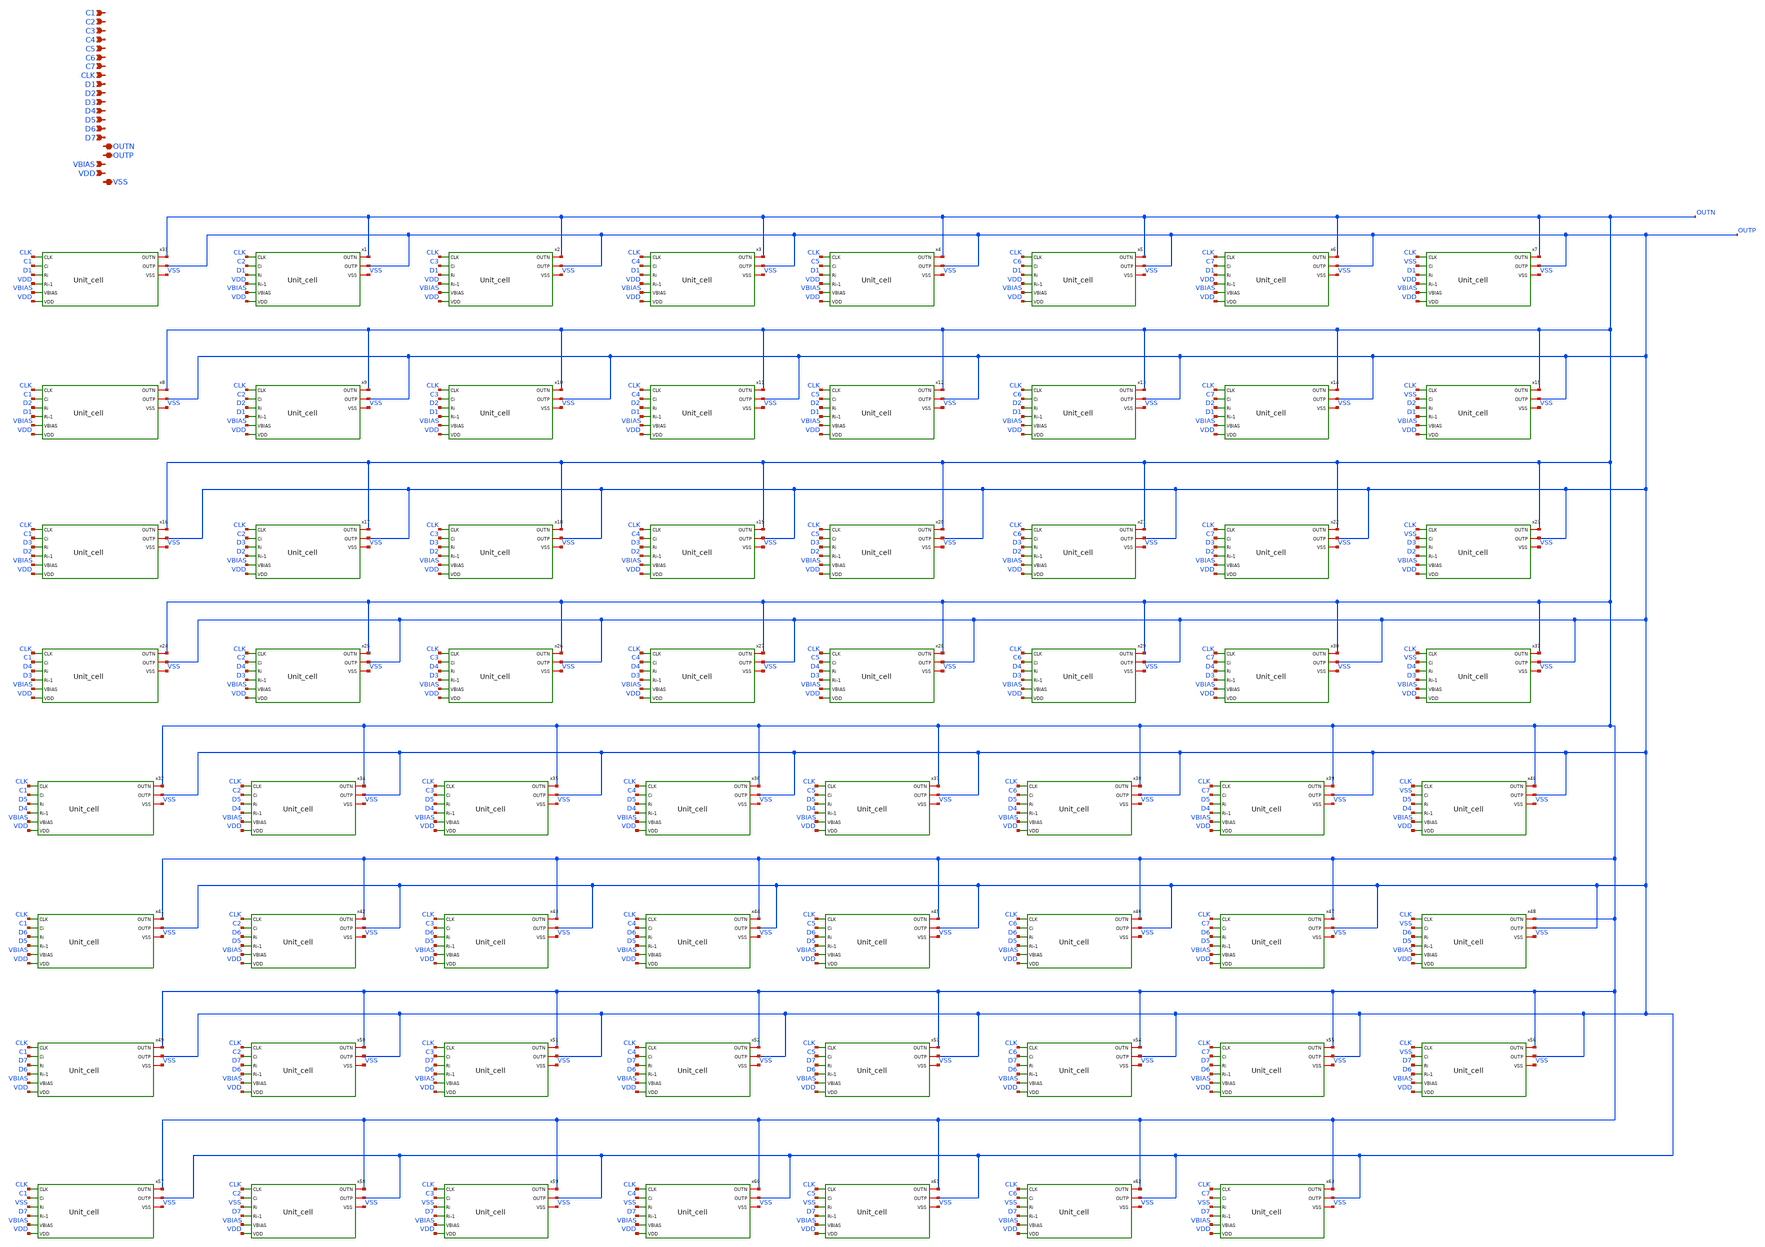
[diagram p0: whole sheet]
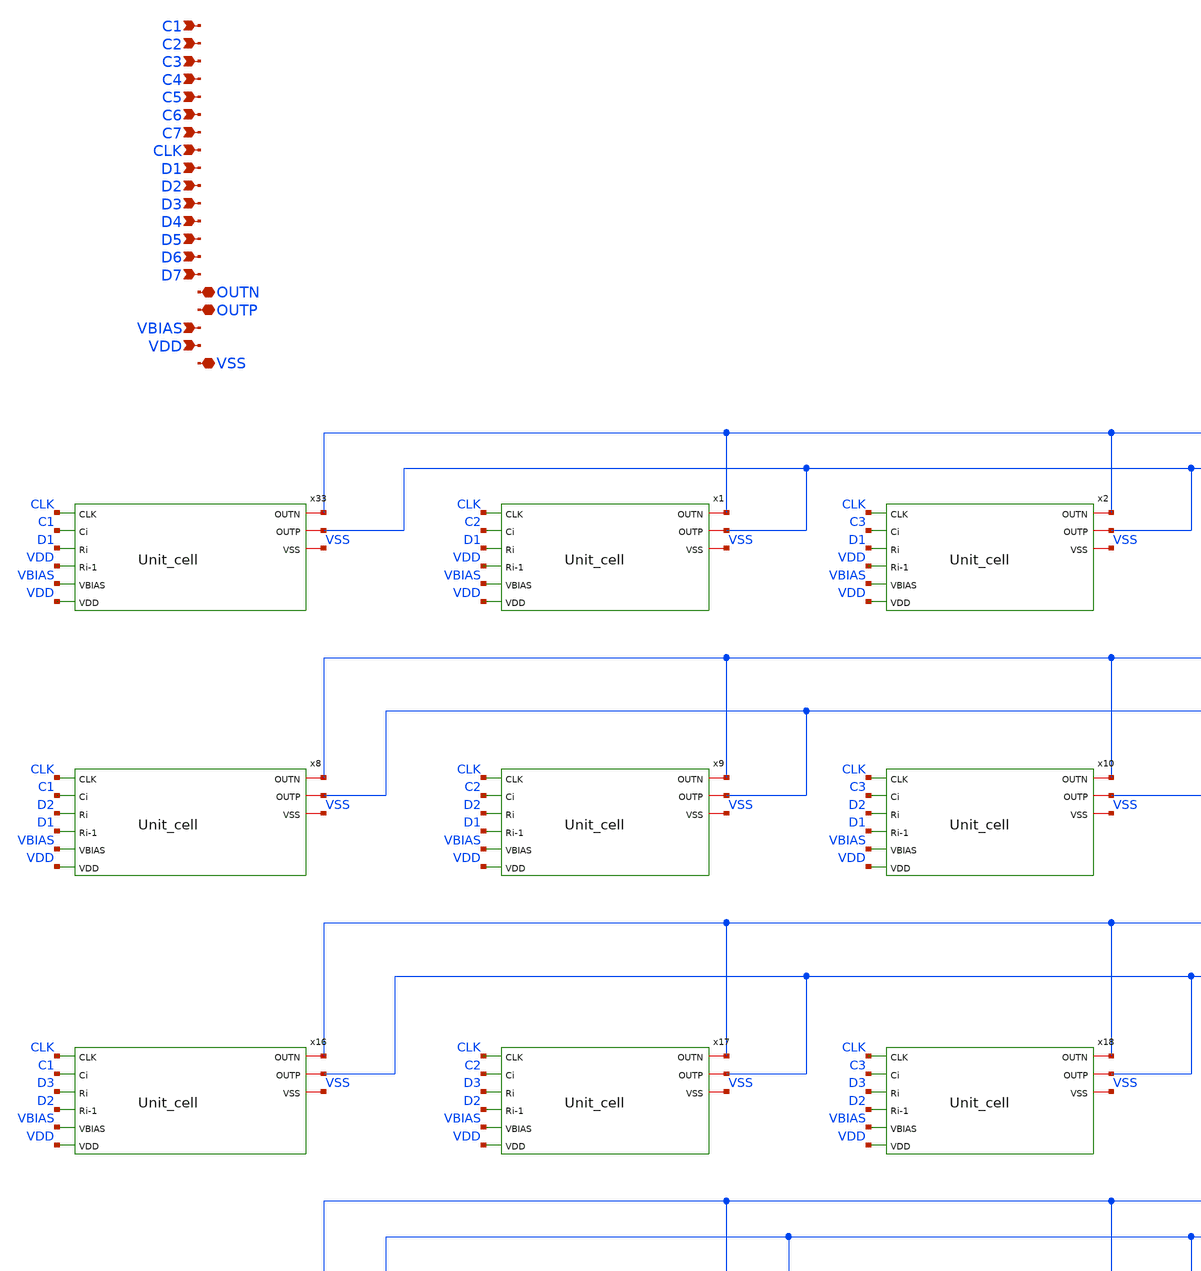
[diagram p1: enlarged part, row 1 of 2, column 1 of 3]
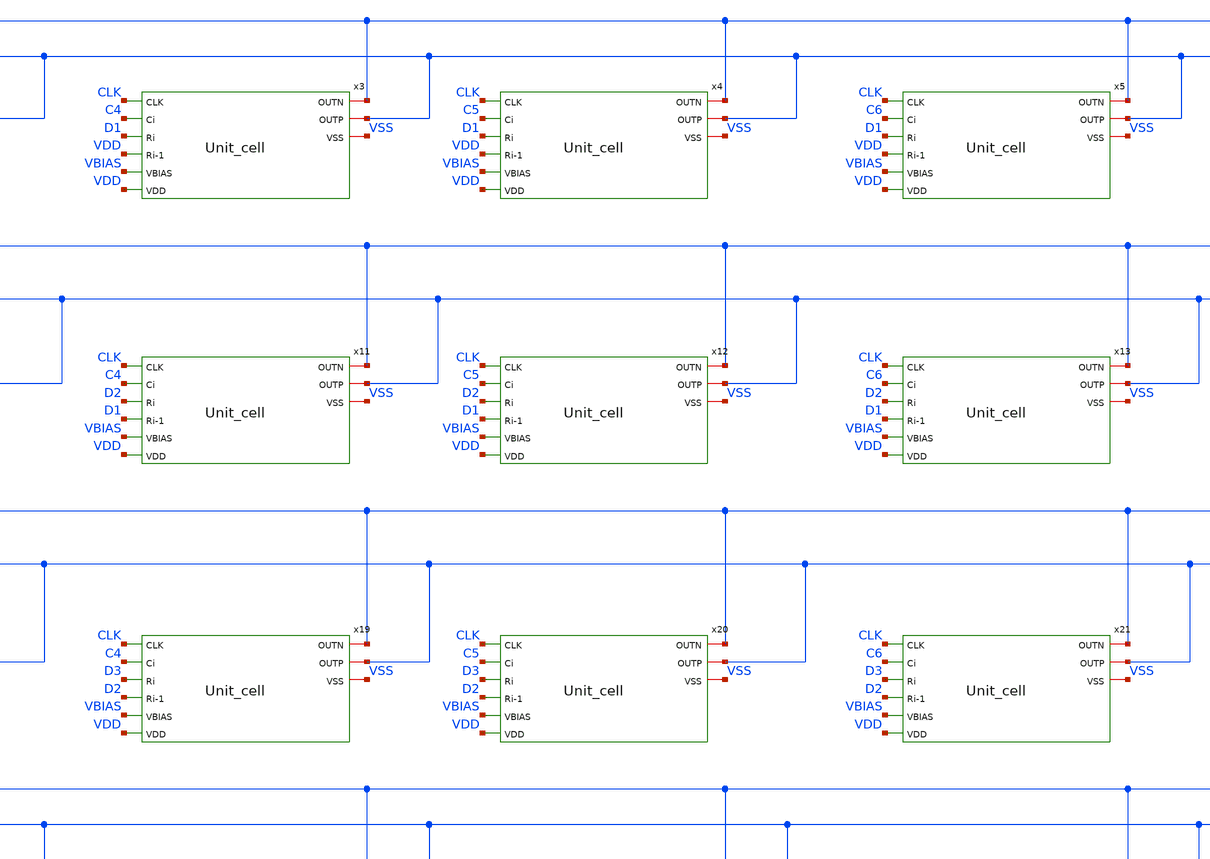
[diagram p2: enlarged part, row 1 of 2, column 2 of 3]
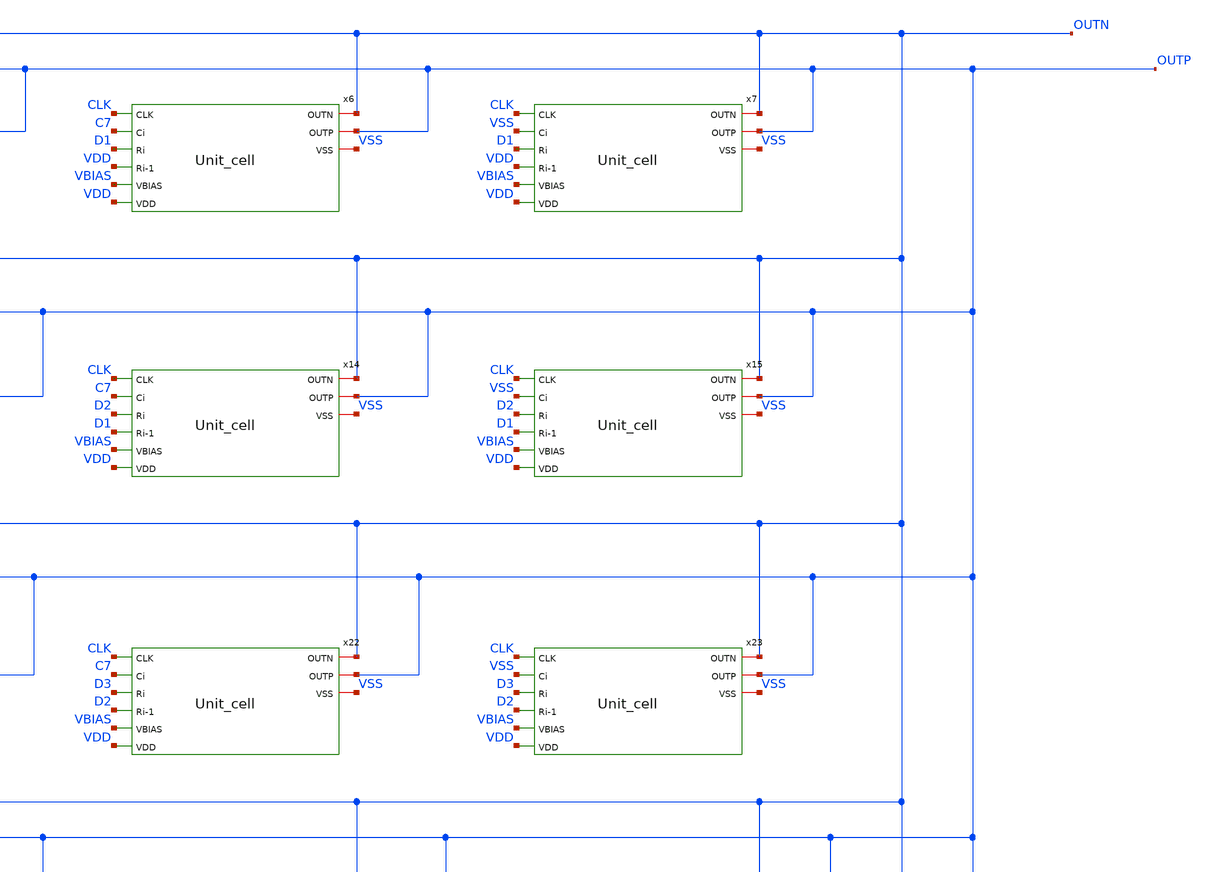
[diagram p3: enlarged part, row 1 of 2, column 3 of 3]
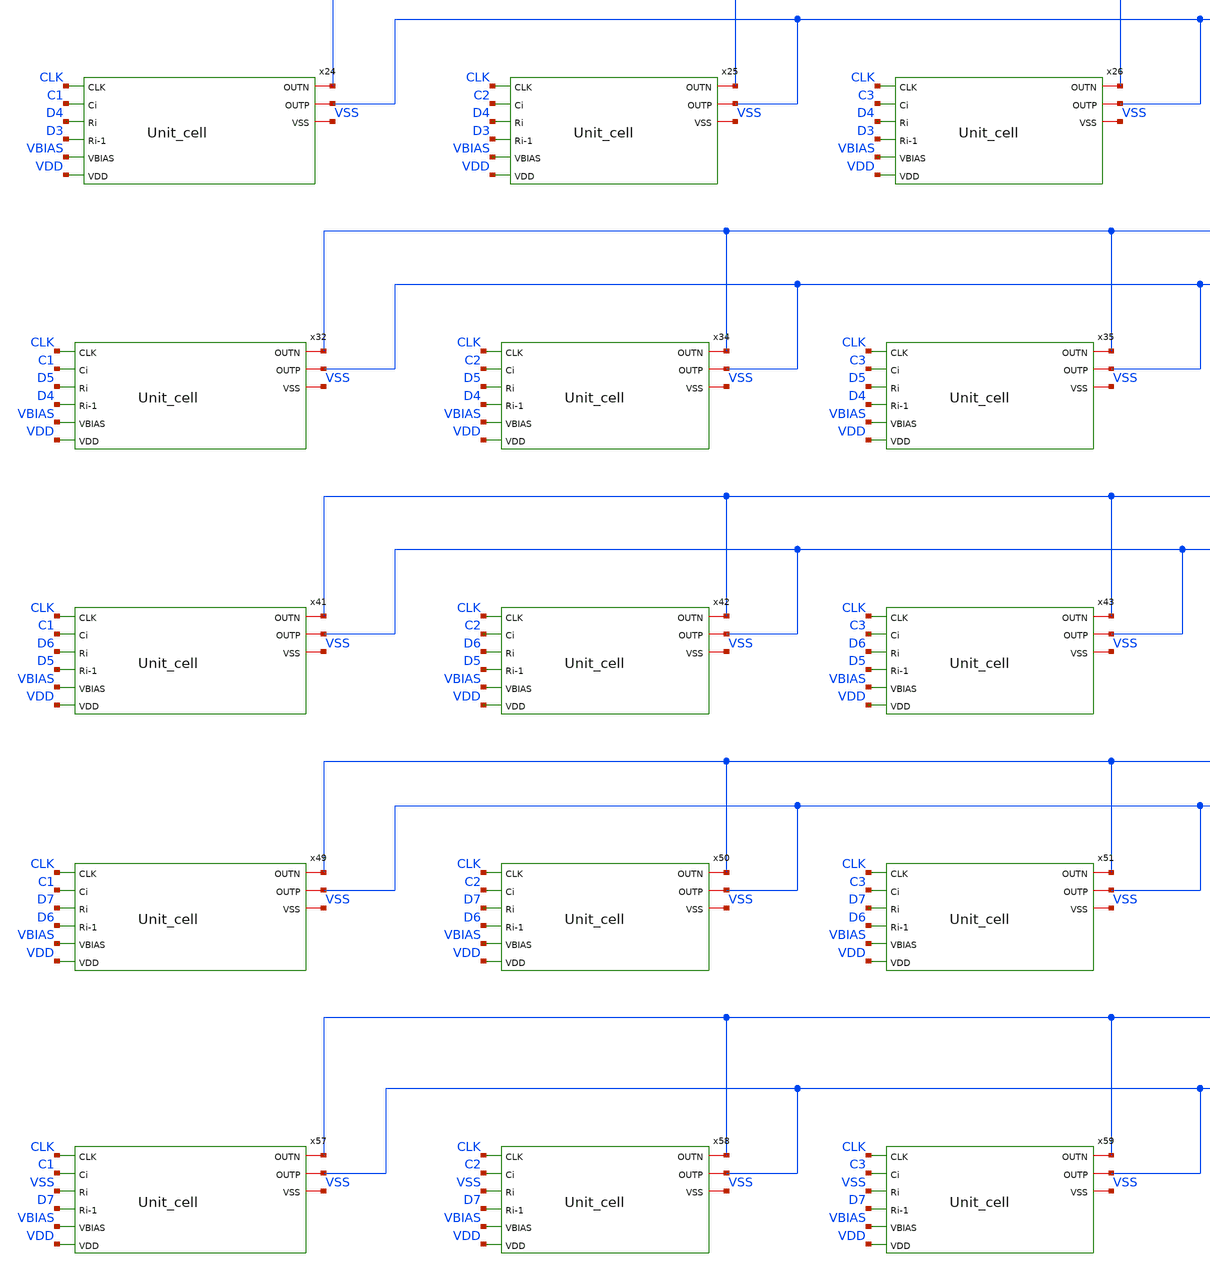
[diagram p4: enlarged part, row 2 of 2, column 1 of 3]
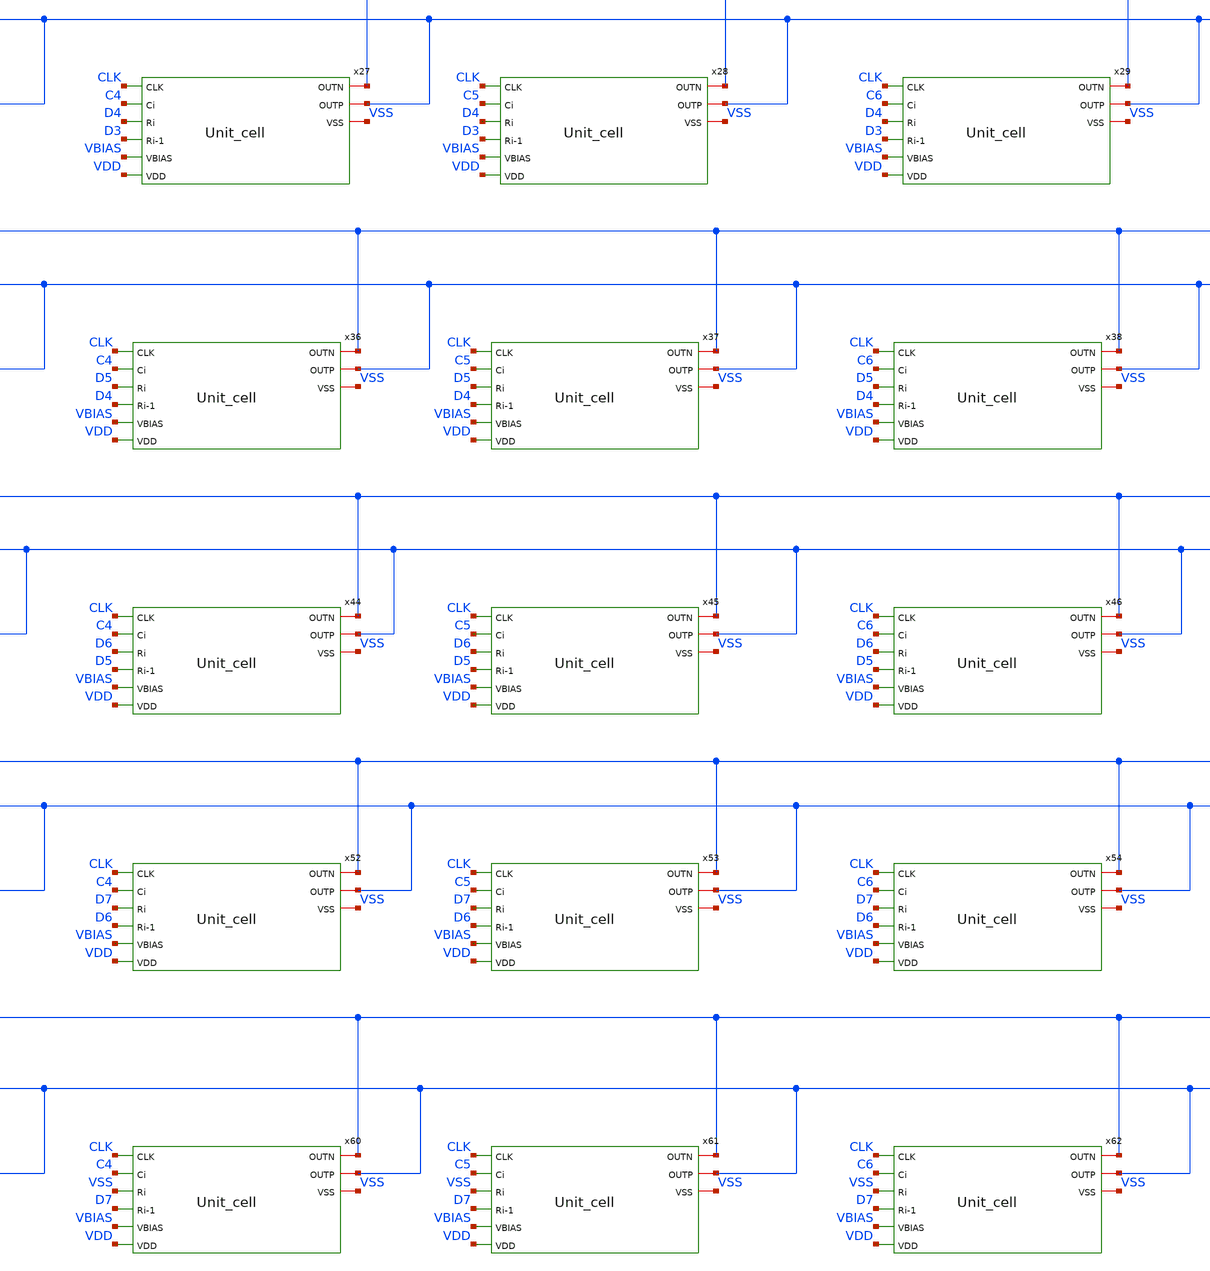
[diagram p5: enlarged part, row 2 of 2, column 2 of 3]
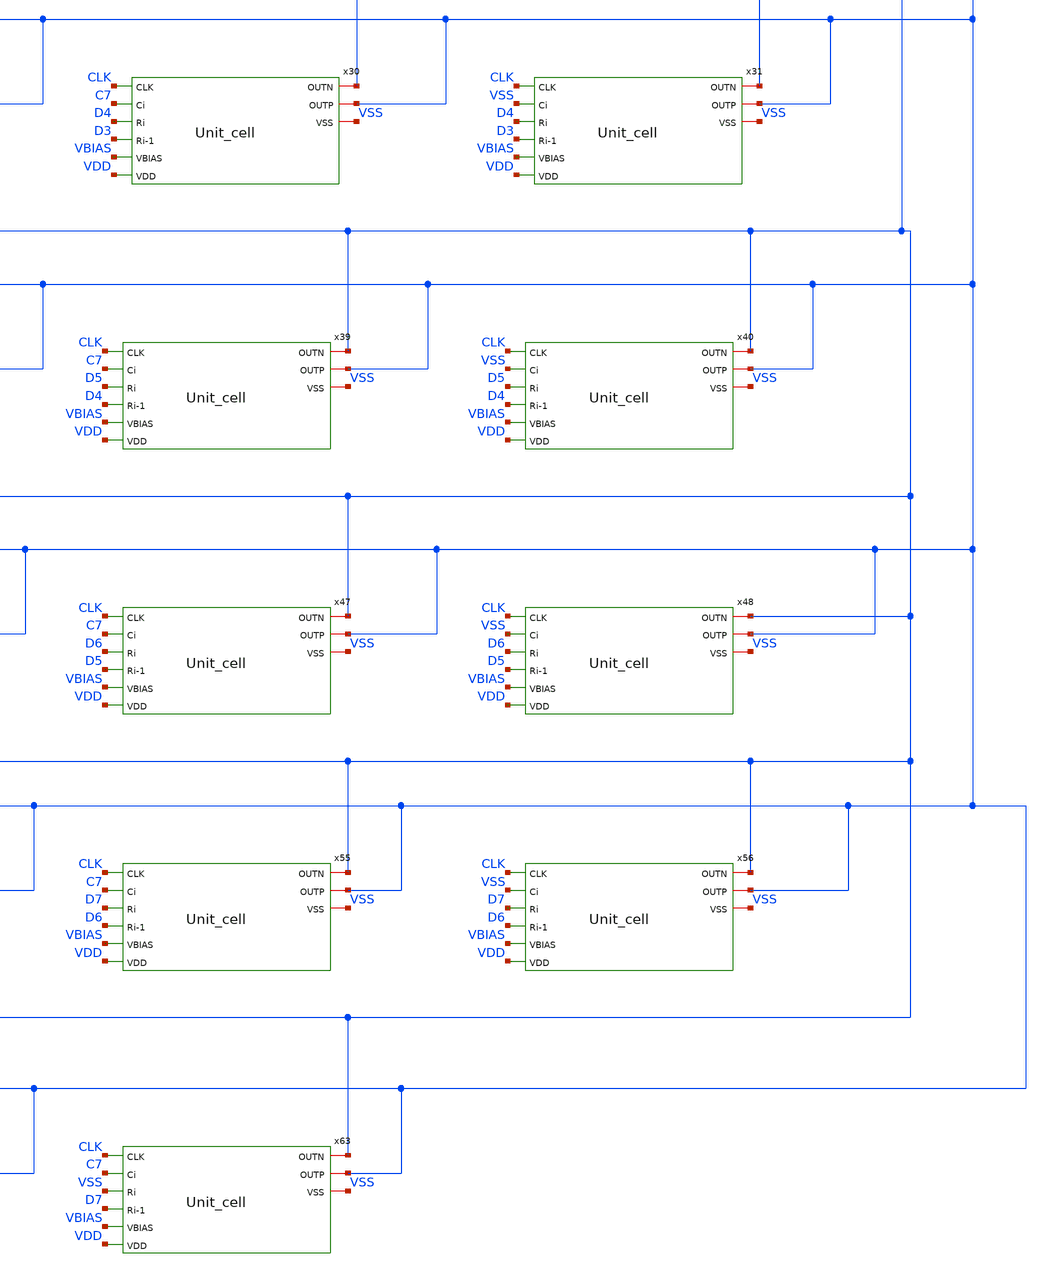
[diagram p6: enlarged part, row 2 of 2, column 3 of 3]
** sch_path: klayout/xschem/6MSB.sch
* IHP-GmbH/IHP-Open-PDK/ihp-sg13g2/libs.tech/xschem/sg13g2_stdcells/sg13g2_or2_2.sch:
* Copyright 2023 IHP PDK Authors
* Licensed under the Apache License, Version 2.0 (the "License");
**.subckt 6MSB VSS VDD VBIAS OUTP OUTN D7 D6 D5 D4 D3 D2 D1 CLK C7 C6 C5 C4 C3 C2 C1
*.iopin VSS
*.ipin VDD
*.ipin VBIAS
*.iopin OUTP
*.iopin OUTN
*.ipin D7
*.ipin D6
*.ipin D5
*.ipin D4
*.ipin D3
*.ipin D2
*.ipin D1
*.ipin CLK
*.ipin C7
*.ipin C6
*.ipin C5
*.ipin C4
*.ipin C3
*.ipin C2
*.ipin C1
x33 CLK C1 OUTN OUTP D1 VDD VBIAS VDD VSS Unit_cell
x1 CLK C2 OUTN OUTP D1 VDD VBIAS VDD VSS Unit_cell
x2 CLK C3 OUTN OUTP D1 VDD VBIAS VDD VSS Unit_cell
x3 CLK C4 OUTN OUTP D1 VDD VBIAS VDD VSS Unit_cell
x4 CLK C5 OUTN OUTP D1 VDD VBIAS VDD VSS Unit_cell
x5 CLK C6 OUTN OUTP D1 VDD VBIAS VDD VSS Unit_cell
x6 CLK C7 OUTN OUTP D1 VDD VBIAS VDD VSS Unit_cell
x7 CLK VSS OUTN OUTP D1 VDD VBIAS VDD VSS Unit_cell
x8 CLK C1 OUTN OUTP D2 D1 VBIAS VDD VSS Unit_cell
x9 CLK C2 OUTN OUTP D2 D1 VBIAS VDD VSS Unit_cell
x10 CLK C3 OUTN OUTP D2 D1 VBIAS VDD VSS Unit_cell
x11 CLK C4 OUTN OUTP D2 D1 VBIAS VDD VSS Unit_cell
x12 CLK C5 OUTN OUTP D2 D1 VBIAS VDD VSS Unit_cell
x13 CLK C6 OUTN OUTP D2 D1 VBIAS VDD VSS Unit_cell
x14 CLK C7 OUTN OUTP D2 D1 VBIAS VDD VSS Unit_cell
x15 CLK VSS OUTN OUTP D2 D1 VBIAS VDD VSS Unit_cell
x16 CLK C1 OUTN OUTP D3 D2 VBIAS VDD VSS Unit_cell
x17 CLK C2 OUTN OUTP D3 D2 VBIAS VDD VSS Unit_cell
x18 CLK C3 OUTN OUTP D3 D2 VBIAS VDD VSS Unit_cell
x19 CLK C4 OUTN OUTP D3 D2 VBIAS VDD VSS Unit_cell
x20 CLK C5 OUTN OUTP D3 D2 VBIAS VDD VSS Unit_cell
x21 CLK C6 OUTN OUTP D3 D2 VBIAS VDD VSS Unit_cell
x22 CLK C7 OUTN OUTP D3 D2 VBIAS VDD VSS Unit_cell
x23 CLK VSS OUTN OUTP D3 D2 VBIAS VDD VSS Unit_cell
x24 CLK C1 OUTN OUTP D4 D3 VBIAS VDD VSS Unit_cell
x25 CLK C2 OUTN OUTP D4 D3 VBIAS VDD VSS Unit_cell
x26 CLK C3 OUTN OUTP D4 D3 VBIAS VDD VSS Unit_cell
x27 CLK C4 OUTN OUTP D4 D3 VBIAS VDD VSS Unit_cell
x28 CLK C5 OUTN OUTP D4 D3 VBIAS VDD VSS Unit_cell
x29 CLK C6 OUTN OUTP D4 D3 VBIAS VDD VSS Unit_cell
x30 CLK C7 OUTN OUTP D4 D3 VBIAS VDD VSS Unit_cell
x31 CLK VSS OUTN OUTP D4 D3 VBIAS VDD VSS Unit_cell
x32 CLK C1 OUTN OUTP D5 D4 VBIAS VDD VSS Unit_cell
x34 CLK C2 OUTN OUTP D5 D4 VBIAS VDD VSS Unit_cell
x35 CLK C3 OUTN OUTP D5 D4 VBIAS VDD VSS Unit_cell
x36 CLK C4 OUTN OUTP D5 D4 VBIAS VDD VSS Unit_cell
x37 CLK C5 OUTN OUTP D5 D4 VBIAS VDD VSS Unit_cell
x38 CLK C6 OUTN OUTP D5 D4 VBIAS VDD VSS Unit_cell
x39 CLK C7 OUTN OUTP D5 D4 VBIAS VDD VSS Unit_cell
x40 CLK VSS OUTN OUTP D5 D4 VBIAS VDD VSS Unit_cell
x41 CLK C1 OUTN OUTP D6 D5 VBIAS VDD VSS Unit_cell
x42 CLK C2 OUTN OUTP D6 D5 VBIAS VDD VSS Unit_cell
x43 CLK C3 OUTN OUTP D6 D5 VBIAS VDD VSS Unit_cell
x44 CLK C4 OUTN OUTP D6 D5 VBIAS VDD VSS Unit_cell
x45 CLK C5 OUTN OUTP D6 D5 VBIAS VDD VSS Unit_cell
x46 CLK C6 OUTN OUTP D6 D5 VBIAS VDD VSS Unit_cell
x47 CLK C7 OUTN OUTP D6 D5 VBIAS VDD VSS Unit_cell
x48 CLK VSS OUTN OUTP D6 D5 VBIAS VDD VSS Unit_cell
x49 CLK C1 OUTN OUTP D7 D6 VBIAS VDD VSS Unit_cell
x50 CLK C2 OUTN OUTP D7 D6 VBIAS VDD VSS Unit_cell
x51 CLK C3 OUTN OUTP D7 D6 VBIAS VDD VSS Unit_cell
x52 CLK C4 OUTN OUTP D7 D6 VBIAS VDD VSS Unit_cell
x53 CLK C5 OUTN OUTP D7 D6 VBIAS VDD VSS Unit_cell
x54 CLK C6 OUTN OUTP D7 D6 VBIAS VDD VSS Unit_cell
x55 CLK C7 OUTN OUTP D7 D6 VBIAS VDD VSS Unit_cell
x56 CLK VSS OUTN OUTP D7 D6 VBIAS VDD VSS Unit_cell
x57 CLK C1 OUTN OUTP VSS D7 VBIAS VDD VSS Unit_cell
x58 CLK C2 OUTN OUTP VSS D7 VBIAS VDD VSS Unit_cell
x59 CLK C3 OUTN OUTP VSS D7 VBIAS VDD VSS Unit_cell
x60 CLK C4 OUTN OUTP VSS D7 VBIAS VDD VSS Unit_cell
x61 CLK C5 OUTN OUTP VSS D7 VBIAS VDD VSS Unit_cell
x62 CLK C6 OUTN OUTP VSS D7 VBIAS VDD VSS Unit_cell
x63 CLK C7 OUTN OUTP VSS D7 VBIAS VDD VSS Unit_cell
**.ends

* expanding   symbol:  Unit_cell.sym # of pins=9
** sym_path: Unit_cell.sym
** sch_path: Unit_cell.sch
.subckt Unit_cell CLK Ci OUTN OUTP Ri Ri-1 VBIAS VDD VSS
*.iopin VSS
*.ipin VDD
*.ipin VBIAS
*.ipin Ri-1
*.ipin Ri
*.iopin OUTP
*.iopin OUTN
*.ipin Ci
*.ipin CLK
x1 net5 net7 OUTN OUTP VBIAS VSS CS_Switch_16x
x2 net1 Ri Ci VDD VSS sg13g2_or2_2
x3 net4 net1 Ri-1 VDD VSS sg13g2_nand2_2
x6 net2 net6 CLK net3 VDD VDD VSS sg13g2_dfrbp_2
C1 OUTP GND 1u m=1
C2 OUTN GND 1u m=1
x4 net7 net2 VDD VSS sg13g2_buf_2
x5 net5 net6 VDD VSS sg13g2_buf_2
x7 net3 net4 VDD VSS sg13g2_buf_2
.ends


* expanding   symbol:  CS_Switch_16x.sym # of pins=6
** sym_path: CS_Switch_16x.sym
** sch_path: CS_Switch_16x.sch
.subckt CS_Switch_16x INN INP OUTN OUTP VBIAS VSS
*.iopin VSS
*.ipin VBIAS
*.iopin OUTP
*.iopin OUTN
*.ipin INP
*.ipin INN
XM1 OUTP INP net1 VSS sg13_lv_nmos w=1u l=0.13u ng=1 m=1 mm_ok=1
XM2 OUTP INP net1 VSS sg13_lv_nmos w=1u l=0.13u ng=1 m=1 mm_ok=1
XM3 OUTN INN net1 VSS sg13_lv_nmos w=1u l=0.13u ng=1 m=1 mm_ok=1
XM4 OUTN INN net1 VSS sg13_lv_nmos w=1u l=0.13u ng=1 m=1 mm_ok=1
XM7 net1 VBIAS net2 VSS sg13_hv_nmos w=5.2u l=0.45u ng=1 m=1 mm_ok=1
XM5 net2 VBIAS VSS VSS sg13_hv_nmos w=5.2u l=0.45u ng=1 m=1 mm_ok=1
C2 net1 GND 1u m=1
.ends


* expanding   symbol:  sg13g2_stdcells/sg13g2_or2_2.sym # of pins=3
** sym_path: sg13g2_stdcells/sg13g2_or2_2.sym
** sch_path: sg13g2_stdcells/sg13g2_or2_2.sch
.subckt sg13g2_or2_2 X A B VDD VSS
*.opin X
*.ipin B
*.ipin A
*.iopin VDD
*.iopin VSS
XM1 net1 B VSS VSS sg13_lv_nmos w=550.00n l=130.00n ng=1 m=1 mm_ok=1
XM2 net1 A VSS VSS sg13_lv_nmos w=550.00n l=130.00n ng=1 m=1 mm_ok=1
XM3 X net1 VSS VSS sg13_lv_nmos w=1.48u l=130.00n ng=2 m=1 mm_ok=1
XM4 net2 A VDD VDD sg13_lv_pmos w=840.00n l=130.00n ng=1 m=1 mm_ok=1
XM5 net1 B net2 VDD sg13_lv_pmos w=840.00n l=130.00n ng=1 m=1 mm_ok=1
XM6 X net1 VDD VDD sg13_lv_pmos w=2.24u l=130.00n ng=2 m=1 mm_ok=1
.ends


* expanding   symbol:  sg13g2_stdcells/sg13g2_nand2_2.sym # of pins=3
** sym_path: sg13g2_stdcells/sg13g2_nand2_2.sym
** sch_path: sg13g2_stdcells/sg13g2_nand2_2.sch
.subckt sg13g2_nand2_2 Y A B VDD VSS
*.iopin VDD
*.iopin VSS
*.opin Y
*.ipin B
*.ipin A
XM1 Y A net1 VSS sg13_lv_nmos w=1.44u l=130.00n ng=2 m=1 mm_ok=1
XM2 net1 B VSS VSS sg13_lv_nmos w=1.44u l=130.00n ng=2 m=1 mm_ok=1
XM3 Y A VDD VDD sg13_lv_pmos w=2.24u l=130.00n ng=2 m=1 mm_ok=1
XM4 Y B VDD VDD sg13_lv_pmos w=2.24u l=130.00n ng=2 m=1 mm_ok=1
.ends


* expanding   symbol:  sg13g2_stdcells/sg13g2_dfrbp_2.sym # of pins=5
** sym_path: sg13g2_stdcells/sg13g2_dfrbp_2.sym
** sch_path: sg13g2_stdcells/sg13g2_dfrbp_2.sch
.subckt sg13g2_dfrbp_2 Q Q_N CLK D RESET_B VDD VSS
*.ipin D
*.ipin RESET_B
*.ipin CLK
*.opin Q
*.opin Q_N
*.iopin VDD
*.iopin VSS
XM1 Db D net12 VSS sg13_lv_nmos w=420.00n l=130.00n ng=1 m=1 mm_ok=1
XM2 net12 RESET_B VSS VSS sg13_lv_nmos w=420.00n l=130.00n ng=1 m=1 mm_ok=1
XM3 net2 clkneg net11 VSS sg13_lv_nmos w=420.00n l=130.00n ng=1 m=1 mm_ok=1
XM4 net11 net3 VSS VSS sg13_lv_nmos w=420.00n l=130.00n ng=1 m=1 mm_ok=1
XM5 net3 net2 net7 VSS sg13_lv_nmos w=420.00n l=130.00n ng=1 m=1 mm_ok=1
XM6 net7 RESET_B VSS VSS sg13_lv_nmos w=420.00n l=130.00n ng=1 m=1 mm_ok=1
XM7 Q_N net2 VSS VSS sg13_lv_nmos w=1.48u l=130.00n ng=2 m=1 mm_ok=1
XM8 net1 net2 VSS VSS sg13_lv_nmos w=640.00n l=130.00n ng=1 m=1 mm_ok=1
XM9 Q net1 VSS VSS sg13_lv_nmos w=1.48u l=130.00n ng=2 m=1 mm_ok=1
XM10 clkneg CLK VSS VSS sg13_lv_nmos w=740.00n l=130.00n ng=1 m=1 mm_ok=1
XM11 clkpos clkneg VSS VSS sg13_lv_nmos w=740.00n l=130.00n ng=1 m=1 mm_ok=1
XM12 Db clkneg net4 VSS sg13_lv_nmos w=420.00n l=130.00n ng=1 m=1 mm_ok=1
XM13 net4 clkpos net10 VSS sg13_lv_nmos w=420.00n l=130.00n ng=1 m=1 mm_ok=1
XM14 net10 net5 net6 VSS sg13_lv_nmos w=420.00n l=130.00n ng=1 m=1 mm_ok=1
XM15 net6 RESET_B VSS VSS sg13_lv_nmos w=420.00n l=130.00n ng=1 m=1 mm_ok=1
XM16 net5 net4 VSS VSS sg13_lv_nmos w=740.00n l=130.00n ng=1 m=1 mm_ok=1
XM17 net5 clkpos net2 VSS sg13_lv_nmos w=740.00n l=130.00n ng=1 m=1 mm_ok=1
XM18 Db RESET_B VDD VDD sg13_lv_pmos w=420.00n l=130.00n ng=1 m=1 mm_ok=1
XM19 Db D VDD VDD sg13_lv_pmos w=420.00n l=130.00n ng=1 m=1 mm_ok=1
XM20 net9 net3 VDD VDD sg13_lv_pmos w=420.00n l=130.00n ng=1 m=1 mm_ok=1
XM21 net2 clkpos net9 VDD sg13_lv_pmos w=420.00n l=130.00n ng=1 m=1 mm_ok=1
XM22 net3 net2 VDD VDD sg13_lv_pmos w=420.00n l=130.00n ng=1 m=1 mm_ok=1
XM23 net3 RESET_B VDD VDD sg13_lv_pmos w=420.00n l=130.00n ng=1 m=1 mm_ok=1
XM24 Q_N net2 VDD VDD sg13_lv_pmos w=2.24u l=130.00n ng=2 m=1 mm_ok=1
XM25 net1 net2 VDD VDD sg13_lv_pmos w=1.000u l=130.00n ng=1 m=1 mm_ok=1
XM26 Q net1 VDD VDD sg13_lv_pmos w=2.24u l=130.00n ng=2 m=1 mm_ok=1
XM27 clkneg CLK VDD VDD sg13_lv_pmos w=1.12u l=130.00n ng=1 m=1 mm_ok=1
XM28 clkpos clkneg VDD VDD sg13_lv_pmos w=1.12u l=130.00n ng=1 m=1 mm_ok=1
XM29 Db clkpos net4 VDD sg13_lv_pmos w=420.00n l=130.00n ng=1 m=1 mm_ok=1
XM30 net8 net5 VDD VDD sg13_lv_pmos w=420.00n l=130.00n ng=1 m=1 mm_ok=1
XM31 net4 clkneg net8 VDD sg13_lv_pmos w=420.00n l=130.00n ng=1 m=1 mm_ok=1
XM32 net4 RESET_B VDD VDD sg13_lv_pmos w=420.00n l=130.00n ng=1 m=1 mm_ok=1
XM33 net5 net4 VDD VDD sg13_lv_pmos w=1.000u l=130.00n ng=1 m=1 mm_ok=1
XM34 net5 clkneg net2 VDD sg13_lv_pmos w=1.000u l=130.00n ng=1 m=1 mm_ok=1
.ends


* expanding   symbol:  sg13g2_stdcells/sg13g2_buf_2.sym # of pins=2
** sym_path: sg13g2_stdcells/sg13g2_buf_2.sym
** sch_path: sg13g2_stdcells/sg13g2_buf_2.sch
.subckt sg13g2_buf_2 X A VDD VSS
*.ipin A
*.opin X
*.iopin VDD
*.iopin VSS
XM1 net1 A VSS VSS sg13_lv_nmos w=640.00n l=130.00n ng=1 m=1 mm_ok=1
XM2 X net1 VSS VSS sg13_lv_nmos w=1.48u l=130.00n ng=2 m=1 mm_ok=1
XM3 net1 A VDD VDD sg13_lv_pmos w=1.000u l=130.00n ng=1 m=1 mm_ok=1
XM4 X net1 VDD VDD sg13_lv_pmos w=2.24u l=130.00n ng=2 m=1 mm_ok=1
.ends

.GLOBAL GND
.end
